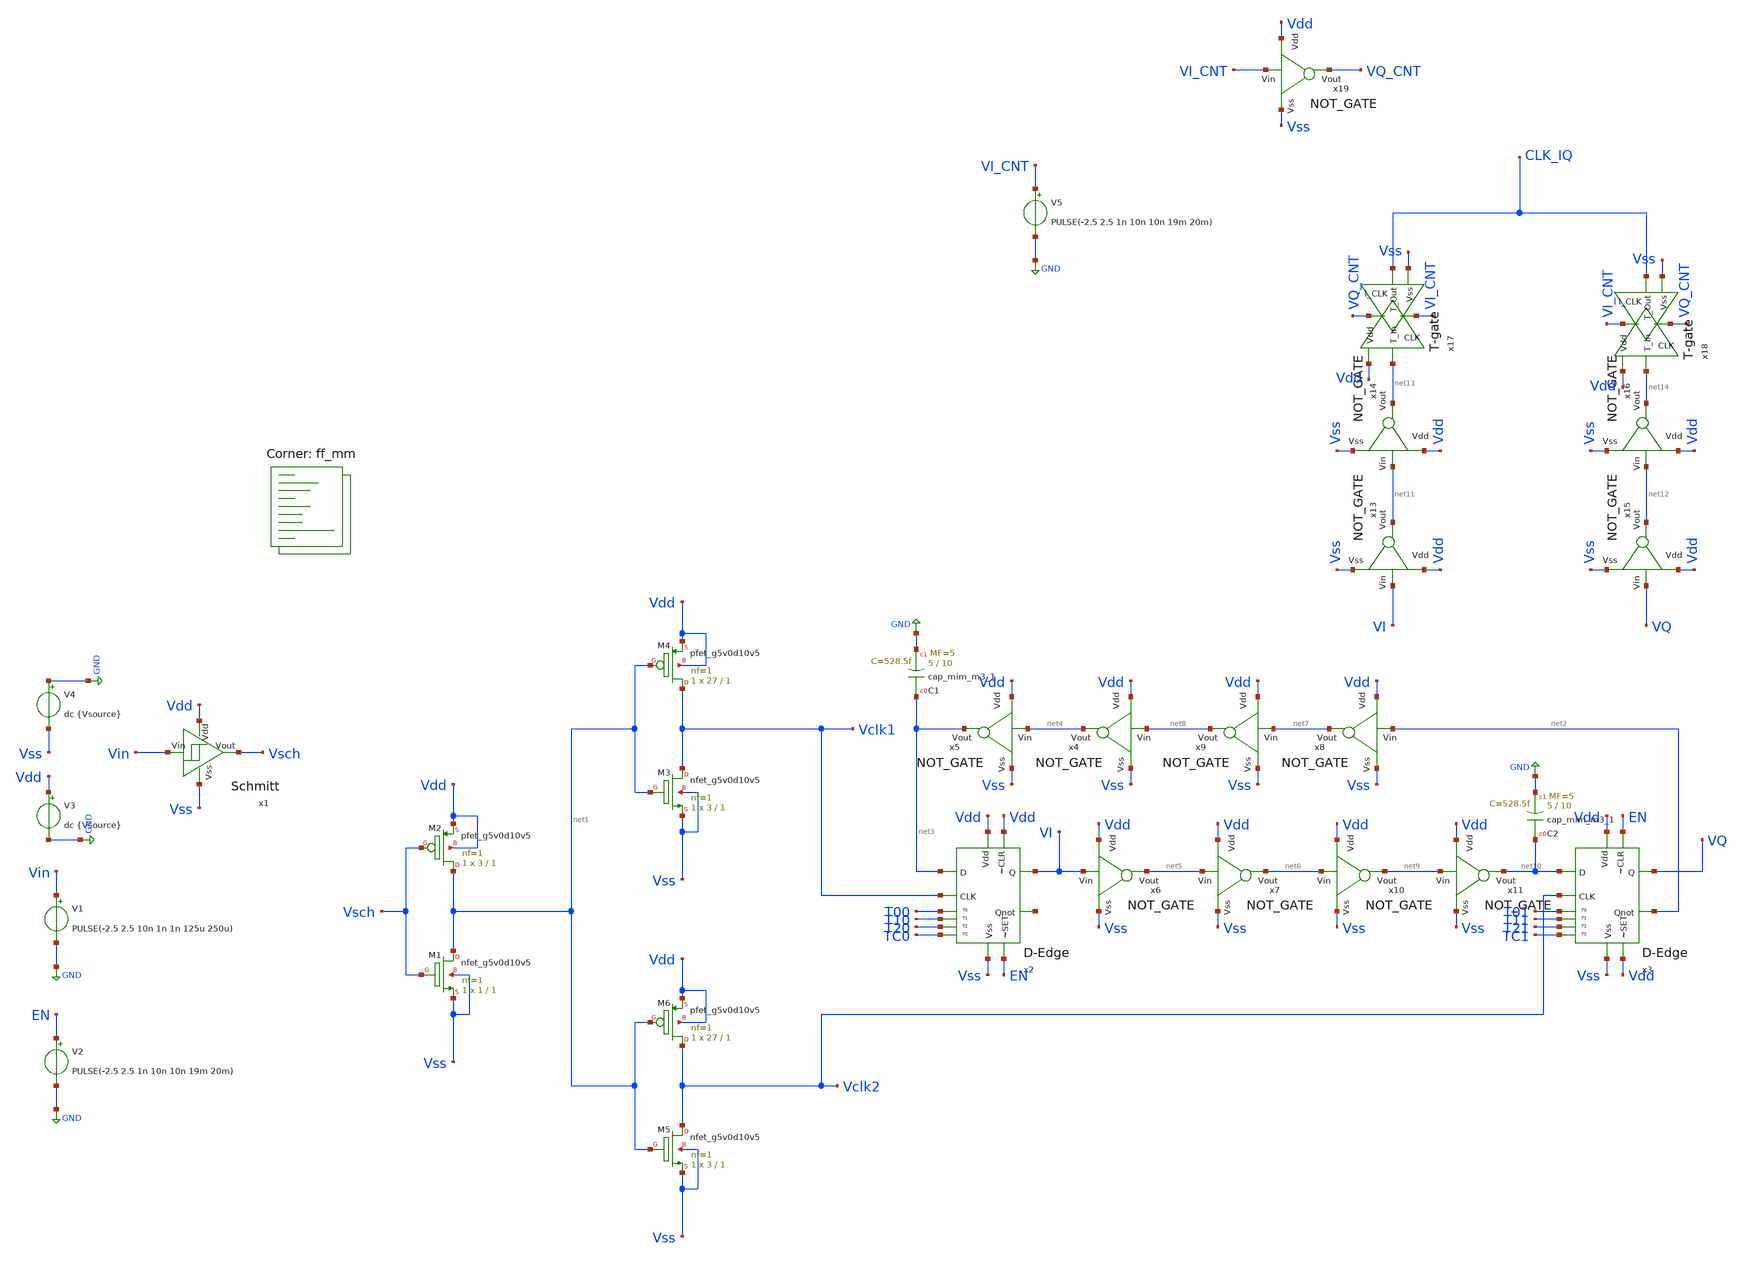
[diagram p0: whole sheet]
** sch_path: xschem/CLK_TB.sch
**.subckt CLK_TB
x1 Vdd Vss Vin Vsch Schmitt
V4 GND Vss dc {Vsource}
V3 Vdd GND dc {Vsource}
V1 Vin GND PULSE(-2.5 2.5 10n 1n 1n 125u 250u)
XM1 net1 Vsch Vss Vss sky130_fd_pr__nfet_g5v0d10v5 L=1 W=1 nf=1 ad='int((1 + 1)/2) * 1 / 1 * 0.29' as='int((1 + 2)/2) * 1 / 1 * 0.29'
+ pd='2*int((1 + 1)/2) * (1 / 1 + 0.29)' ps='2*int((1 + 2)/2) * (1 / 1 + 0.29)' nrd='0.29 / 1 ' nrs='0.29 / 1 '
+ sa=0 sb=0 sd=0 mult=1 m=1
XM2 net1 Vsch Vdd Vdd sky130_fd_pr__pfet_g5v0d10v5 L=1 W=3 nf=1 ad='int((1 + 1)/2) * 3 / 1 * 0.29' as='int((1 + 2)/2) * 3 / 1 * 0.29'
+ pd='2*int((1 + 1)/2) * (3 / 1 + 0.29)' ps='2*int((1 + 2)/2) * (3 / 1 + 0.29)' nrd='0.29 / 3 ' nrs='0.29 / 3 '
+ sa=0 sb=0 sd=0 mult=1 m=1
XM3 Vclk1 net1 Vss Vss sky130_fd_pr__nfet_g5v0d10v5 L=1 W=3 nf=1 ad='int((1 + 1)/2) * 3 / 1 * 0.29' as='int((1 + 2)/2) * 3 / 1 * 0.29'
+ pd='2*int((1 + 1)/2) * (3 / 1 + 0.29)' ps='2*int((1 + 2)/2) * (3 / 1 + 0.29)' nrd='0.29 / 3 ' nrs='0.29 / 3 '
+ sa=0 sb=0 sd=0 mult=1 m=1
XM4 Vclk1 net1 Vdd Vdd sky130_fd_pr__pfet_g5v0d10v5 L=1 W=27 nf=1 ad='int((1 + 1)/2) * 27 / 1 * 0.29'
+ as='int((1 + 2)/2) * 27 / 1 * 0.29' pd='2*int((1 + 1)/2) * (27 / 1 + 0.29)' ps='2*int((1 + 2)/2) * (27 / 1 + 0.29)'
+ nrd='0.29 / 27 ' nrs='0.29 / 27 ' sa=0 sb=0 sd=0 mult=1 m=1
XM5 Vclk2 net1 Vss Vss sky130_fd_pr__nfet_g5v0d10v5 L=1 W=3 nf=1 ad='int((1 + 1)/2) * 3 / 1 * 0.29' as='int((1 + 2)/2) * 3 / 1 * 0.29'
+ pd='2*int((1 + 1)/2) * (3 / 1 + 0.29)' ps='2*int((1 + 2)/2) * (3 / 1 + 0.29)' nrd='0.29 / 3 ' nrs='0.29 / 3 '
+ sa=0 sb=0 sd=0 mult=1 m=1
XM6 Vclk2 net1 Vdd Vdd sky130_fd_pr__pfet_g5v0d10v5 L=1 W=27 nf=1 ad='int((1 + 1)/2) * 27 / 1 * 0.29'
+ as='int((1 + 2)/2) * 27 / 1 * 0.29' pd='2*int((1 + 1)/2) * (27 / 1 + 0.29)' ps='2*int((1 + 2)/2) * (27 / 1 + 0.29)'
+ nrd='0.29 / 27 ' nrs='0.29 / 27 ' sa=0 sb=0 sd=0 mult=1 m=1
x2 Vdd Vss Vdd EN VI net3 net15 Vclk1 TC0 T20 T10 T00 D-Edge
x3 Vdd Vss EN Vdd VQ net10 net2 Vclk2 TC1 T21 T11 T01 D-Edge
x4 Vdd net4 net8 Vss NOT_GATE
x5 Vdd net3 net4 Vss NOT_GATE
x6 Vdd net5 VI Vss NOT_GATE
x7 Vdd net6 net5 Vss NOT_GATE
V2 EN GND PULSE(-2.5 2.5 1n 10n 10n 19m 20m)
x8 Vdd net7 net2 Vss NOT_GATE
x9 Vdd net8 net7 Vss NOT_GATE
x10 Vdd net9 net6 Vss NOT_GATE
x11 Vdd net10 net9 Vss NOT_GATE
x13 Vdd net11 VI Vss NOT_GATE
x14 Vdd net13 net11 Vss NOT_GATE
x15 Vdd net12 VQ Vss NOT_GATE
x16 Vdd net14 net12 Vss NOT_GATE
x17 VQ_CNT net13 CLK_IQ Vdd Vss VI_CNT T-gate
x18 VI_CNT net14 CLK_IQ Vdd Vss VQ_CNT T-gate
x19 Vdd VQ_CNT VI_CNT Vss NOT_GATE
V5 VI_CNT GND PULSE(-2.5 2.5 1n 10n 10n 19m 20m)
XC1 net3 GND sky130_fd_pr__cap_mim_m3_1 W=5 L=10 MF=5 m=5
XC2 net10 GND sky130_fd_pr__cap_mim_m3_1 W=5 L=10 MF=5 m=5
**** begin user architecture code
.lib $::SKYWATER_MODELS/sky130.lib.spice ff_mm






.options method = gear
.options klu
***Centered at 40C and varies to a range of -20 to 100; with 20C being 1-standard dev***
.param TEMPGAUSS = agauss(40, 60, 3)

***Centered at 2.5V and varies to a range of 2V to 3V; with 0.16mV being 1-standard dev***
.param VOLTGAUSS = agauss(2.5, 0.5, 3)

.param ptemp = 'TEMPGAUSS'

.param Vsource = 'VOLTGAUSS'
.options temp = {ptemp}

.csparam ctemp = {ptemp}
.csparam cvolt = {Vsource}


.control
 let T = 27
 let V = 2.5

 let i_count = 10

 let index = 0

 set wr_vecnames
 dowhile index <= 10
   save all
   tran 1u 10m uic

   write CLK_TB_FF_MM_PVT.raw

   set noprintscale

   set appendwrite


   let V = $&cvolt
   let T = $&ctemp

   echo -n This is $&V
   echo -n This is $&T
   echo -n This is $&index

   let index = index + 1
   reset
 end
  **OL AC
  *** print col GAIN_vec UGW_vec PM_vec T_vec V_vec > FDA_AC_CM_GAIN_UGW_PM_SS_PVT.txt
  **Offset
   *** print col OFFSETDIF_vec OFFSETMIX_vec OFFSETOUT_vec T_vec V_vec >
+ PRE_LPF_OFFSETS_SS_MM_PVT.txt

.endc
.end


**** end user architecture code
**.ends

* expanding   symbol:  Schmitt.sym # of pins=4
** sym_path: xschem/Schmitt.sym
** sch_path: xschem/Schmitt.sch
.subckt Schmitt Vdd Vss Vin Vout
*.opin Vout
*.ipin Vin
*.ipin Vdd
*.ipin Vss
XM1 net1 Vin Vss Vss sky130_fd_pr__nfet_g5v0d10v5 L=0.5 W=2.92 nf=1 ad='int((1 + 1)/2) * 2.92 / 1 * 0.29'
+ as='int((1 + 2)/2) * 2.92 / 1 * 0.29' pd='2*int((1 + 1)/2) * (2.92 / 1 + 0.29)' ps='2*int((1 + 2)/2) * (2.92 / 1 + 0.29)'
+ nrd='0.29 / 2.92 ' nrs='0.29 / 2.92 ' sa=0 sb=0 sd=0 mult=1 m=1
XM5 net2 Vin Vdd Vdd sky130_fd_pr__pfet_g5v0d10v5 L=0.5 W=9.78 nf=1 ad='int((1 + 1)/2) * 9.78 / 1 * 0.29'
+ as='int((1 + 2)/2) * 9.78 / 1 * 0.29' pd='2*int((1 + 1)/2) * (9.78 / 1 + 0.29)' ps='2*int((1 + 2)/2) * (9.78 / 1 + 0.29)'
+ nrd='0.29 / 9.78 ' nrs='0.29 / 9.78 ' sa=0 sb=0 sd=0 mult=1 m=1
XM3 Vdd Vout net1 Vss sky130_fd_pr__nfet_g5v0d10v5 L=0.5 W=1 nf=1 ad='int((1 + 1)/2) * 1 / 1 * 0.29'
+ as='int((1 + 2)/2) * 1 / 1 * 0.29' pd='2*int((1 + 1)/2) * (1 / 1 + 0.29)' ps='2*int((1 + 2)/2) * (1 / 1 + 0.29)'
+ nrd='0.29 / 1 ' nrs='0.29 / 1 ' sa=0 sb=0 sd=0 mult=1 m=1
XM2 Vout Vin net1 Vss sky130_fd_pr__nfet_g5v0d10v5 L=0.5 W=4 nf=1 ad='int((1 + 1)/2) * 4 / 1 * 0.29'
+ as='int((1 + 2)/2) * 4 / 1 * 0.29' pd='2*int((1 + 1)/2) * (4 / 1 + 0.29)' ps='2*int((1 + 2)/2) * (4 / 1 + 0.29)'
+ nrd='0.29 / 4 ' nrs='0.29 / 4 ' sa=0 sb=0 sd=0 mult=1 m=1
XM6 Vss Vout net2 Vdd sky130_fd_pr__pfet_g5v0d10v5 L=0.5 W=3 nf=1 ad='int((1 + 1)/2) * 3 / 1 * 0.29'
+ as='int((1 + 2)/2) * 3 / 1 * 0.29' pd='2*int((1 + 1)/2) * (3 / 1 + 0.29)' ps='2*int((1 + 2)/2) * (3 / 1 + 0.29)'
+ nrd='0.29 / 3 ' nrs='0.29 / 3 ' sa=0 sb=0 sd=0 mult=1 m=1
XM4 Vout Vin net2 Vdd sky130_fd_pr__pfet_g5v0d10v5 L=0.5 W=12 nf=1 ad='int((1 + 1)/2) * 12 / 1 * 0.29'
+ as='int((1 + 2)/2) * 12 / 1 * 0.29' pd='2*int((1 + 1)/2) * (12 / 1 + 0.29)' ps='2*int((1 + 2)/2) * (12 / 1 + 0.29)'
+ nrd='0.29 / 12 ' nrs='0.29 / 12 ' sa=0 sb=0 sd=0 mult=1 m=1
.ends


* expanding   symbol:  D-Edge.sym # of pins=12
** sym_path: xschem/D-Edge.sym
** sch_path: xschem/D-Edge.sch
.subckt D-Edge Vdd Vss ~CLR ~SET Q D Qnot CLK TC T2 T1 T0
*.ipin D
*.ipin Vdd
*.ipin Vss
*.opin Q
*.opin Qnot
*.ipin ~CLR
*.ipin ~SET
*.ipin CLK
*.opin T0
*.opin T1
*.opin T2
*.opin TC
x1 CLK D T1 Vdd Vss CLK_I T-gate
x3 CLK_I T0 T1 Vdd Vss CLK T-gate
x4 CLK_I net1 T2 Vdd Vss CLK T-gate
x8 CLK Qnot T2 Vdd Vss CLK_I T-gate
x11 Vdd ~CLR T1 net1 Vss NAND_GATE
x2 Vdd ~SET net1 T0 Vss NAND_GATE
x5 Vdd ~CLR T2 Q Vss NAND_GATE
x7 Vdd ~SET Q Qnot Vss NAND_GATE
XM1 CLK_I CLK Vss Vss sky130_fd_pr__nfet_g5v0d10v5 L=1 W=3 nf=1 ad='int((1 + 1)/2) * 3 / 1 * 0.29' as='int((1 + 2)/2) * 3 / 1 * 0.29'
+ pd='2*int((1 + 1)/2) * (3 / 1 + 0.29)' ps='2*int((1 + 2)/2) * (3 / 1 + 0.29)' nrd='0.29 / 3 ' nrs='0.29 / 3 '
+ sa=0 sb=0 sd=0 mult=1 m=1
XM2 CLK_I CLK Vdd Vdd sky130_fd_pr__pfet_g5v0d10v5 L=1 W=27 nf=1 ad='int((1 + 1)/2) * 27 / 1 * 0.29'
+ as='int((1 + 2)/2) * 27 / 1 * 0.29' pd='2*int((1 + 1)/2) * (27 / 1 + 0.29)' ps='2*int((1 + 2)/2) * (27 / 1 + 0.29)'
+ nrd='0.29 / 27 ' nrs='0.29 / 27 ' sa=0 sb=0 sd=0 mult=1 m=1
XM3 TC CLK_I Vss Vss sky130_fd_pr__nfet_g5v0d10v5 L=1 W=3 nf=1 ad='int((1 + 1)/2) * 3 / 1 * 0.29' as='int((1 + 2)/2) * 3 / 1 * 0.29'
+ pd='2*int((1 + 1)/2) * (3 / 1 + 0.29)' ps='2*int((1 + 2)/2) * (3 / 1 + 0.29)' nrd='0.29 / 3 ' nrs='0.29 / 3 '
+ sa=0 sb=0 sd=0 mult=1 m=1
XM4 TC CLK_I Vdd Vdd sky130_fd_pr__pfet_g5v0d10v5 L=1 W=27 nf=1 ad='int((1 + 1)/2) * 27 / 1 * 0.29' as='int((1 + 2)/2) * 27 / 1 * 0.29'
+ pd='2*int((1 + 1)/2) * (27 / 1 + 0.29)' ps='2*int((1 + 2)/2) * (27 / 1 + 0.29)' nrd='0.29 / 27 ' nrs='0.29 / 27 '
+ sa=0 sb=0 sd=0 mult=1 m=1
.ends


* expanding   symbol:  NOT_GATE.sym # of pins=4
** sym_path: xschem/NOT_GATE.sym
** sch_path: xschem/NOT_GATE.sch
.subckt NOT_GATE Vdd Vout Vin Vss
*.opin Vout
*.ipin Vdd
*.ipin Vss
*.ipin Vin
XM1 Vout Vin Vss Vss sky130_fd_pr__nfet_g5v0d10v5 L=1 W=1 nf=1 ad='int((1 + 1)/2) * 1 / 1 * 0.29' as='int((1 + 2)/2) * 1 / 1 * 0.29'
+ pd='2*int((1 + 1)/2) * (1 / 1 + 0.29)' ps='2*int((1 + 2)/2) * (1 / 1 + 0.29)' nrd='0.29 / 1 ' nrs='0.29 / 1 '
+ sa=0 sb=0 sd=0 mult=1 m=1
XM2 Vout Vin Vdd Vdd sky130_fd_pr__pfet_g5v0d10v5 L=1 W=3 nf=1 ad='int((1 + 1)/2) * 3 / 1 * 0.29' as='int((1 + 2)/2) * 3 / 1 * 0.29'
+ pd='2*int((1 + 1)/2) * (3 / 1 + 0.29)' ps='2*int((1 + 2)/2) * (3 / 1 + 0.29)' nrd='0.29 / 3 ' nrs='0.29 / 3 '
+ sa=0 sb=0 sd=0 mult=1 m=1
.ends


* expanding   symbol:  T-gate.sym # of pins=6
** sym_path: xschem/T-gate.sym
** sch_path: xschem/T-gate.sch
.subckt T-gate I_CLK T_In T_Out Vdd Vss CLK
*.ipin T_In
*.opin T_Out
*.ipin Vdd
*.ipin Vss
*.ipin I_CLK
*.ipin CLK
XM1 T_In I_CLK T_Out Vdd sky130_fd_pr__pfet_g5v0d10v5 L=0.5 W=3 nf=1 ad='int((1 + 1)/2) * 3 / 1 * 0.29'
+ as='int((1 + 2)/2) * 3 / 1 * 0.29' pd='2*int((1 + 1)/2) * (3 / 1 + 0.29)' ps='2*int((1 + 2)/2) * (3 / 1 + 0.29)'
+ nrd='0.29 / 3 ' nrs='0.29 / 3 ' sa=0 sb=0 sd=0 mult=1 m=1
XM3 T_Out CLK T_In Vss sky130_fd_pr__nfet_g5v0d10v5 L=0.5 W=1 nf=1 ad='int((1 + 1)/2) * 1 / 1 * 0.29'
+ as='int((1 + 2)/2) * 1 / 1 * 0.29' pd='2*int((1 + 1)/2) * (1 / 1 + 0.29)' ps='2*int((1 + 2)/2) * (1 / 1 + 0.29)'
+ nrd='0.29 / 1 ' nrs='0.29 / 1 ' sa=0 sb=0 sd=0 mult=1 m=1
XM2 T_Out CLK T_Out Vdd sky130_fd_pr__pfet_g5v0d10v5 L=0.5 W=1.5 nf=1 ad='int((1 + 1)/2) * 1.5 / 1 * 0.29'
+ as='int((1 + 2)/2) * 1.5 / 1 * 0.29' pd='2*int((1 + 1)/2) * (1.5 / 1 + 0.29)' ps='2*int((1 + 2)/2) * (1.5 / 1 + 0.29)'
+ nrd='0.29 / 1.5 ' nrs='0.29 / 1.5 ' sa=0 sb=0 sd=0 mult=1 m=1
XM4 T_In CLK T_In Vdd sky130_fd_pr__pfet_g5v0d10v5 L=0.5 W=1.5 nf=1 ad='int((1 + 1)/2) * 1.5 / 1 * 0.29'
+ as='int((1 + 2)/2) * 1.5 / 1 * 0.29' pd='2*int((1 + 1)/2) * (1.5 / 1 + 0.29)' ps='2*int((1 + 2)/2) * (1.5 / 1 + 0.29)'
+ nrd='0.29 / 1.5 ' nrs='0.29 / 1.5 ' sa=0 sb=0 sd=0 mult=1 m=1
XM5 T_In I_CLK T_In Vss sky130_fd_pr__nfet_g5v0d10v5 L=0.5 W=0.5 nf=1 ad='int((1 + 1)/2) * 0.5 / 1 * 0.29'
+ as='int((1 + 2)/2) * 0.5 / 1 * 0.29' pd='2*int((1 + 1)/2) * (0.5 / 1 + 0.29)' ps='2*int((1 + 2)/2) * (0.5 / 1 + 0.29)'
+ nrd='0.29 / 0.5 ' nrs='0.29 / 0.5 ' sa=0 sb=0 sd=0 mult=1 m=1
XM6 T_Out I_CLK T_Out Vss sky130_fd_pr__nfet_g5v0d10v5 L=0.5 W=0.5 nf=1 ad='int((1 + 1)/2) * 0.5 / 1 * 0.29'
+ as='int((1 + 2)/2) * 0.5 / 1 * 0.29' pd='2*int((1 + 1)/2) * (0.5 / 1 + 0.29)' ps='2*int((1 + 2)/2) * (0.5 / 1 + 0.29)'
+ nrd='0.29 / 0.5 ' nrs='0.29 / 0.5 ' sa=0 sb=0 sd=0 mult=1 m=1
.ends


* expanding   symbol:  NAND_GATE.sym # of pins=5
** sym_path: xschem/NAND_GATE.sym
** sch_path: xschem/NAND_GATE.sch
.subckt NAND_GATE Vdd A B Vout Vss
*.ipin Vdd
*.ipin Vss
*.ipin A
*.ipin B
*.opin Vout
XM3 Vout A net1 Vss sky130_fd_pr__nfet_g5v0d10v5 L=0.5 W=1 nf=1 ad='int((1 + 1)/2) * 1 / 1 * 0.29' as='int((1 + 2)/2) * 1 / 1 * 0.29'
+ pd='2*int((1 + 1)/2) * (1 / 1 + 0.29)' ps='2*int((1 + 2)/2) * (1 / 1 + 0.29)' nrd='0.29 / 1 ' nrs='0.29 / 1 '
+ sa=0 sb=0 sd=0 mult=1 m=1
XM4 Vout A Vdd Vdd sky130_fd_pr__pfet_g5v0d10v5 L=0.5 W=3 nf=1 ad='int((1 + 1)/2) * 3 / 1 * 0.29' as='int((1 + 2)/2) * 3 / 1 * 0.29'
+ pd='2*int((1 + 1)/2) * (3 / 1 + 0.29)' ps='2*int((1 + 2)/2) * (3 / 1 + 0.29)' nrd='0.29 / 3 ' nrs='0.29 / 3 '
+ sa=0 sb=0 sd=0 mult=1 m=1
XM5 Vout B Vdd Vdd sky130_fd_pr__pfet_g5v0d10v5 L=0.5 W=3 nf=1 ad='int((1 + 1)/2) * 3 / 1 * 0.29' as='int((1 + 2)/2) * 3 / 1 * 0.29'
+ pd='2*int((1 + 1)/2) * (3 / 1 + 0.29)' ps='2*int((1 + 2)/2) * (3 / 1 + 0.29)' nrd='0.29 / 3 ' nrs='0.29 / 3 '
+ sa=0 sb=0 sd=0 mult=1 m=1
XM1 net1 B Vss Vss sky130_fd_pr__nfet_g5v0d10v5 L=0.5 W=1 nf=1 ad='int((1 + 1)/2) * 1 / 1 * 0.29' as='int((1 + 2)/2) * 1 / 1 * 0.29'
+ pd='2*int((1 + 1)/2) * (1 / 1 + 0.29)' ps='2*int((1 + 2)/2) * (1 / 1 + 0.29)' nrd='0.29 / 1 ' nrs='0.29 / 1 '
+ sa=0 sb=0 sd=0 mult=1 m=1
.ends

.GLOBAL GND
.end
